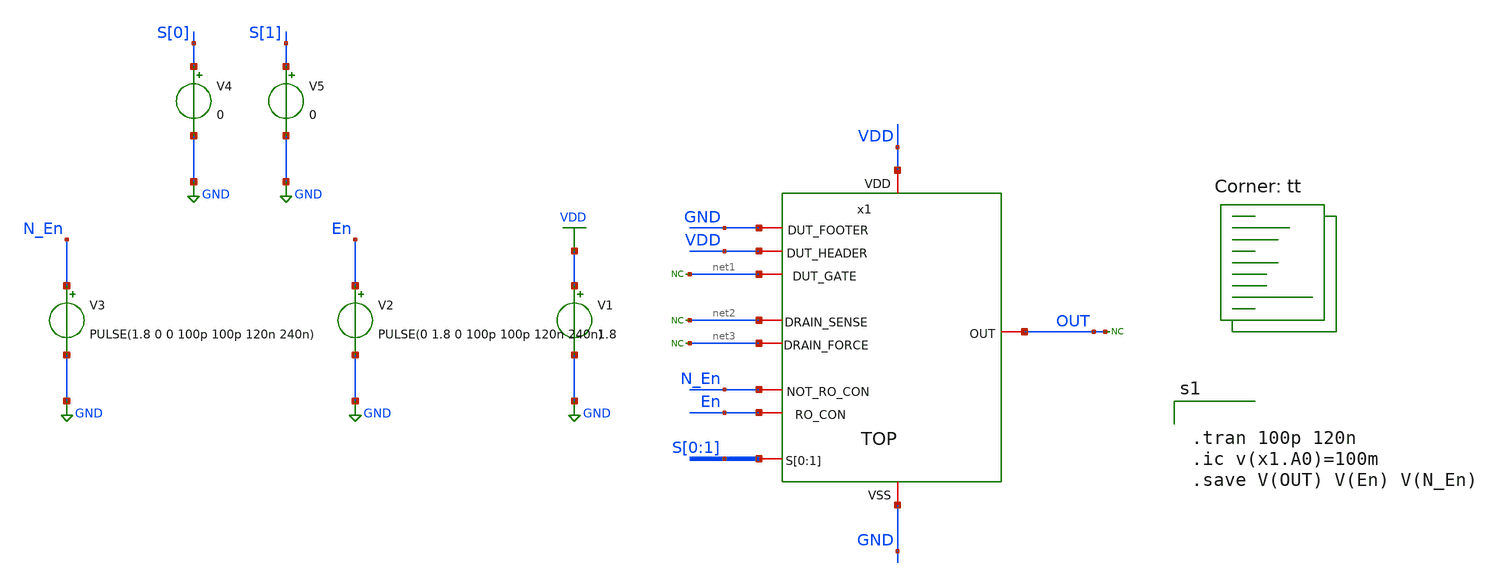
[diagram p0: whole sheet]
** sch_path: TB/TOP_TB.sch
**.subckt TOP_TB
x1 GND VDD VDD GND net1 N_En En net2 OUT net3 S[0] S[1] TOP
V1 VDD GND 1.8
V2 En GND PULSE(0 1.8 0 100p 100p 120n 240n)
V3 N_En GND PULSE(1.8 0 0 100p 100p 120n 240n)
* noconn #net1
* noconn #net2
* noconn #net3
V4 S[0] GND 0
V5 S[1] GND 0
* noconn OUT
**** begin user architecture code


.tran 100p 120n
.ic v(x1.A0)=100m
.save V(OUT) V(En) V(N_En)


 .lib $::SKYWATER_MODELS/sky130.lib.spice tt
.include $::SKYWATER_STDCELLS/sky130_fd_sc_hd.spice

**** end user architecture code
**.ends
.GLOBAL VDD
.GLOBAL GND
.end
